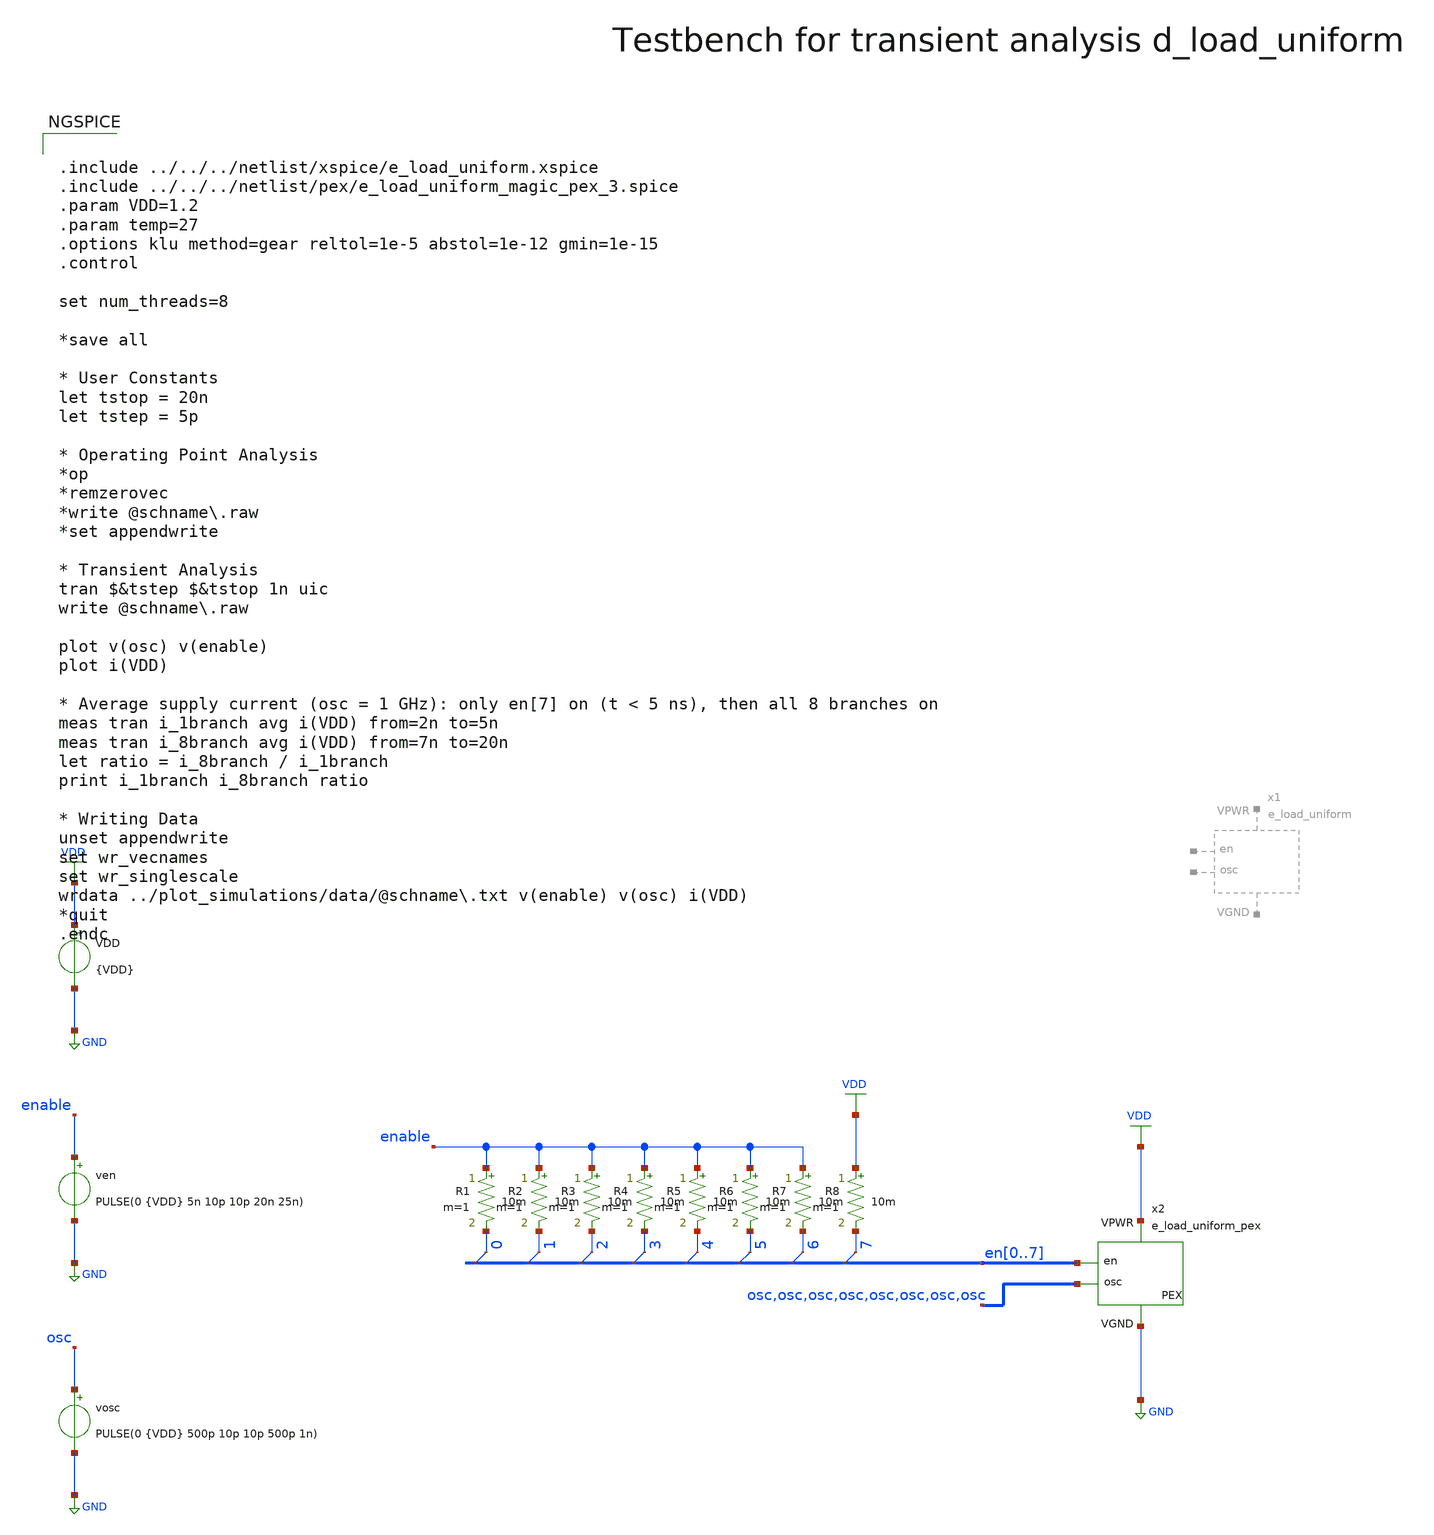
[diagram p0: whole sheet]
** sch_path: macros/heichips26_digital_project/macros/e_load_uniform/testbenches/xschem/e_load_uniform_tb_tran.sch
**.subckt e_load_uniform_tb_tran
VDD VDD GND {VDD}
ven enable GND PULSE(0 {VDD} 5n 10p 10p 20n 25n)
x2 VDD GND osc en0 en1 en2 en3 en4 en5 en6 en7 e_load_uniform_pex
vosc osc GND PULSE(0 {VDD} 500p 10p 10p 500p 1n)
* tap: en[0..7] --> en0
* tap: en[0..7] --> en2
* tap: en[0..7] --> en4
* tap: en[0..7] --> en6
* tap: en[0..7] --> en7
* tap: en[0..7] --> en5
* tap: en[0..7] --> en3
* tap: en[0..7] --> en1
R1 enable en0 10m m=1
R2 enable en1 10m m=1
R3 enable en2 10m m=1
R4 enable en3 10m m=1
R5 enable en4 10m m=1
R6 enable en5 10m m=1
R7 enable en6 10m m=1
R8 VDD en7 10m m=1
**** begin user architecture code


.include ../../../netlist/xspice/e_load_uniform.xspice
.include ../../../netlist/pex/e_load_uniform_magic_pex_3.spice
.param VDD=1.2
.param temp=27
.options klu method=gear reltol=1e-5 abstol=1e-12 gmin=1e-15
.control

set num_threads=8

*save all

* User Constants
let tstop = 20n
let tstep = 5p

* Operating Point Analysis
*op
*remzerovec
*write @schname\.raw
*set appendwrite

* Transient Analysis
tran $&tstep $&tstop 1n uic
write @schname\.raw

plot v(osc) v(enable)
plot i(VDD)

* Average supply current (osc = 1 GHz): only en[7] on (t < 5 ns), then all 8 branches on
meas tran i_1branch avg i(VDD) from=2n to=5n
meas tran i_8branch avg i(VDD) from=7n to=20n
let ratio = i_8branch / i_1branch
print i_1branch i_8branch ratio

* Writing Data
unset appendwrite
set wr_vecnames
set wr_singlescale
wrdata ../plot_simulations/data/@schname\.txt v(enable) v(osc) i(VDD)
*quit
.endc


.lib cornerMOSlv.lib mos_tt
.lib cornerMOShv.lib mos_tt
.lib cornerRES.lib res_typ
.lib cornerDIO.lib dio_tt

**** end user architecture code
**.ends
.GLOBAL GND
.GLOBAL VDD
.end
